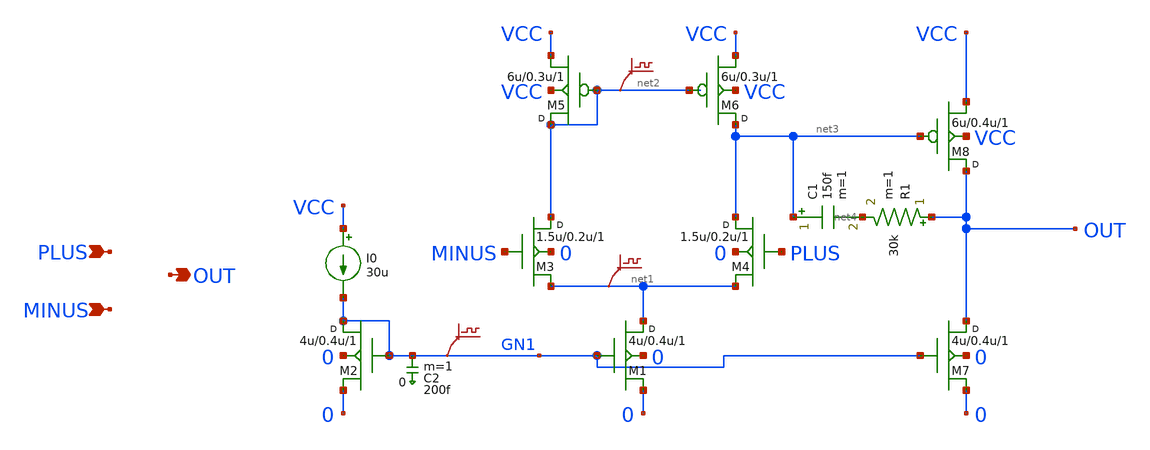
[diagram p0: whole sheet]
** sch_path: xschem_library/ngspice/opamp_65nm.sch
**.subckt opamp_65nm PLUS MINUS OUT
*.ipin PLUS
*.ipin MINUS
*.opin OUT
M1 net1 GN1 0 0 nmos w=4u l=0.4u m=1
M2 GN1 GN1 0 0 nmos w=4u l=0.4u m=1
I0 VCC GN1 30u
M3 net2 MINUS net1 0 nmos w=1.5u l=0.2u m=1
M4 net3 PLUS net1 0 nmos w=1.5u l=0.2u m=1
M5 net2 net2 VCC VCC pmos w=6u l=0.3u m=1
M6 net3 net2 VCC VCC pmos w=6u l=0.3u m=1
M8 OUT net3 VCC VCC pmos w=6u l=0.4u m=1
.save v(gn1)
.save v(net2)
M7 OUT GN1 0 0 nmos w=4u l=0.4u m=1
R1 OUT net4 30k m=1
C1 net3 net4 150f m=1
C2 GN1 0 200f m=1
.save v(net1)
**.ends
.end
